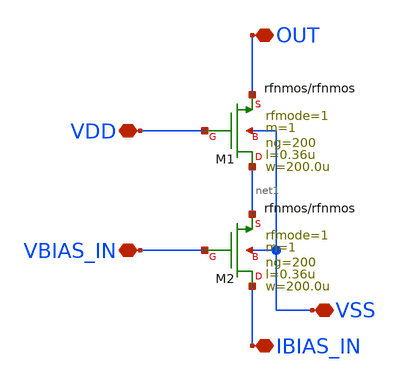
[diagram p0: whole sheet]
** sch_path: GPS_LNA/design_data/lvs/parts/nmos_200_2.sch
**.subckt nmos_200_2 IBIAS_IN VSS OUT VBIAS_IN VDD
*.iopin IBIAS_IN
*.iopin VSS
*.iopin OUT
*.iopin VBIAS_IN
*.iopin VDD
XM2 IBIAS_IN VBIAS_IN net1 VSS rfnmos w=200.0u l=0.36u ng=200 m=1 rfmode=1 mm_ok=1
XM1 net1 VDD OUT VSS rfnmos w=200.0u l=0.36u ng=200 m=1 rfmode=1 mm_ok=1
**.ends
.end
